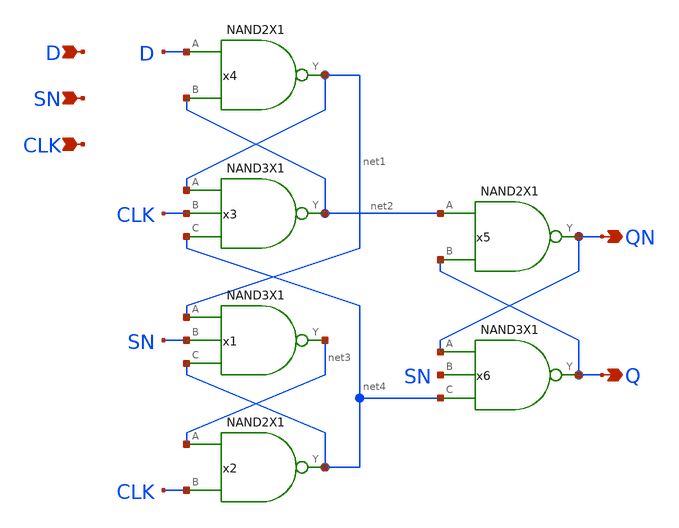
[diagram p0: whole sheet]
** sch_path: lib/xschem/DFFSNX1.sch
**.subckt DFFSNX1 D QN SN CLK Q
*.ipin D
*.opin QN
*.ipin SN
*.ipin CLK
*.opin Q
x1 net3 net1 SN net4 VDD VSS NAND3X1
x2 net4 net3 CLK VDD VSS NAND2X1
x3 net2 net1 CLK net4 VDD VSS NAND3X1
x4 net1 D net2 VDD VSS NAND2X1
x5 QN net2 Q VDD VSS NAND2X1
x6 Q QN SN net4 VDD VSS NAND3X1
**.ends

* expanding   symbol:  NAND3X1.sym # of pins=4
** sym_path: lib/xschem/NAND3X1.sym
** sch_path: lib/xschem/NAND3X1.sch
.subckt NAND3X1 Y A B C VDD VSS
*.ipin A
*.opin Y
*.ipin B
*.ipin C
XM1 net2 C VSS VSS sky130_fd_pr__nfet_01v8 L=0.15 W=3 nf=1 ad='int((nf+1)/2) * W/nf * 0.29' as='int((nf+2)/2) * W/nf * 0.29'
+ pd='2*int((nf+1)/2) * (W/nf + 0.29)' ps='2*int((nf+2)/2) * (W/nf + 0.29)' nrd='0.29 / W' nrs='0.29 / W'
+ sa=0 sb=0 sd=0 mult=1 m=1
XM2 Y A VDD VDD sky130_fd_pr__pfet_01v8 L=0.15 W=2 nf=1 ad='int((nf+1)/2) * W/nf * 0.29' as='int((nf+2)/2) * W/nf * 0.29'
+ pd='2*int((nf+1)/2) * (W/nf + 0.29)' ps='2*int((nf+2)/2) * (W/nf + 0.29)' nrd='0.29 / W' nrs='0.29 / W'
+ sa=0 sb=0 sd=0 mult=1 m=1
XM3 net1 B net2 VSS sky130_fd_pr__nfet_01v8 L=0.15 W=3 nf=1 ad='int((nf+1)/2) * W/nf * 0.29' as='int((nf+2)/2) * W/nf * 0.29'
+ pd='2*int((nf+1)/2) * (W/nf + 0.29)' ps='2*int((nf+2)/2) * (W/nf + 0.29)' nrd='0.29 / W' nrs='0.29 / W'
+ sa=0 sb=0 sd=0 mult=1 m=1
XM4 Y A net1 VSS sky130_fd_pr__nfet_01v8 L=0.15 W=3 nf=1 ad='int((nf+1)/2) * W/nf * 0.29' as='int((nf+2)/2) * W/nf * 0.29'
+ pd='2*int((nf+1)/2) * (W/nf + 0.29)' ps='2*int((nf+2)/2) * (W/nf + 0.29)' nrd='0.29 / W' nrs='0.29 / W'
+ sa=0 sb=0 sd=0 mult=1 m=1
XM5 Y A VDD VDD sky130_fd_pr__pfet_01v8 L=0.15 W=2 nf=1 ad='int((nf+1)/2) * W/nf * 0.29' as='int((nf+2)/2) * W/nf * 0.29'
+ pd='2*int((nf+1)/2) * (W/nf + 0.29)' ps='2*int((nf+2)/2) * (W/nf + 0.29)' nrd='0.29 / W' nrs='0.29 / W'
+ sa=0 sb=0 sd=0 mult=1 m=1
XM6 Y B VDD VDD sky130_fd_pr__pfet_01v8 L=0.15 W=2 nf=1 ad='int((nf+1)/2) * W/nf * 0.29' as='int((nf+2)/2) * W/nf * 0.29'
+ pd='2*int((nf+1)/2) * (W/nf + 0.29)' ps='2*int((nf+2)/2) * (W/nf + 0.29)' nrd='0.29 / W' nrs='0.29 / W'
+ sa=0 sb=0 sd=0 mult=1 m=1
XM7 Y B VDD VDD sky130_fd_pr__pfet_01v8 L=0.15 W=2 nf=1 ad='int((nf+1)/2) * W/nf * 0.29' as='int((nf+2)/2) * W/nf * 0.29'
+ pd='2*int((nf+1)/2) * (W/nf + 0.29)' ps='2*int((nf+2)/2) * (W/nf + 0.29)' nrd='0.29 / W' nrs='0.29 / W'
+ sa=0 sb=0 sd=0 mult=1 m=1
XM8 Y C VDD VDD sky130_fd_pr__pfet_01v8 L=0.15 W=2 nf=1 ad='int((nf+1)/2) * W/nf * 0.29' as='int((nf+2)/2) * W/nf * 0.29'
+ pd='2*int((nf+1)/2) * (W/nf + 0.29)' ps='2*int((nf+2)/2) * (W/nf + 0.29)' nrd='0.29 / W' nrs='0.29 / W'
+ sa=0 sb=0 sd=0 mult=1 m=1
XM9 Y C VDD VDD sky130_fd_pr__pfet_01v8 L=0.15 W=2 nf=1 ad='int((nf+1)/2) * W/nf * 0.29' as='int((nf+2)/2) * W/nf * 0.29'
+ pd='2*int((nf+1)/2) * (W/nf + 0.29)' ps='2*int((nf+2)/2) * (W/nf + 0.29)' nrd='0.29 / W' nrs='0.29 / W'
+ sa=0 sb=0 sd=0 mult=1 m=1
.ends


* expanding   symbol:  NAND2X1.sym # of pins=3
** sym_path: lib/xschem/NAND2X1.sym
** sch_path: lib/xschem/NAND2X1.sch
.subckt NAND2X1 Y A B VDD VSS
*.ipin A
*.opin Y
*.ipin B
XM1 Y A VDD VDD sky130_fd_pr__pfet_01v8 L=0.15 W=2 nf=1 ad='int((nf+1)/2) * W/nf * 0.29' as='int((nf+2)/2) * W/nf * 0.29'
+ pd='2*int((nf+1)/2) * (W/nf + 0.29)' ps='2*int((nf+2)/2) * (W/nf + 0.29)' nrd='0.29 / W' nrs='0.29 / W'
+ sa=0 sb=0 sd=0 mult=1 m=1
XM5 Y A net1 VSS sky130_fd_pr__nfet_01v8 L=0.15 W=3 nf=1 ad='int((nf+1)/2) * W/nf * 0.29' as='int((nf+2)/2) * W/nf * 0.29'
+ pd='2*int((nf+1)/2) * (W/nf + 0.29)' ps='2*int((nf+2)/2) * (W/nf + 0.29)' nrd='0.29 / W' nrs='0.29 / W'
+ sa=0 sb=0 sd=0 mult=1 m=1
XM2 Y A VDD VDD sky130_fd_pr__pfet_01v8 L=0.15 W=2 nf=1 ad='int((nf+1)/2) * W/nf * 0.29' as='int((nf+2)/2) * W/nf * 0.29'
+ pd='2*int((nf+1)/2) * (W/nf + 0.29)' ps='2*int((nf+2)/2) * (W/nf + 0.29)' nrd='0.29 / W' nrs='0.29 / W'
+ sa=0 sb=0 sd=0 mult=1 m=1
XM3 Y B VDD VDD sky130_fd_pr__pfet_01v8 L=0.15 W=2 nf=1 ad='int((nf+1)/2) * W/nf * 0.29' as='int((nf+2)/2) * W/nf * 0.29'
+ pd='2*int((nf+1)/2) * (W/nf + 0.29)' ps='2*int((nf+2)/2) * (W/nf + 0.29)' nrd='0.29 / W' nrs='0.29 / W'
+ sa=0 sb=0 sd=0 mult=1 m=1
XM4 Y B VDD VDD sky130_fd_pr__pfet_01v8 L=0.15 W=2 nf=1 ad='int((nf+1)/2) * W/nf * 0.29' as='int((nf+2)/2) * W/nf * 0.29'
+ pd='2*int((nf+1)/2) * (W/nf + 0.29)' ps='2*int((nf+2)/2) * (W/nf + 0.29)' nrd='0.29 / W' nrs='0.29 / W'
+ sa=0 sb=0 sd=0 mult=1 m=1
XM6 net1 B VSS VSS sky130_fd_pr__nfet_01v8 L=0.15 W=3 nf=1 ad='int((nf+1)/2) * W/nf * 0.29' as='int((nf+2)/2) * W/nf * 0.29'
+ pd='2*int((nf+1)/2) * (W/nf + 0.29)' ps='2*int((nf+2)/2) * (W/nf + 0.29)' nrd='0.29 / W' nrs='0.29 / W'
+ sa=0 sb=0 sd=0 mult=1 m=1
.ends

.end
